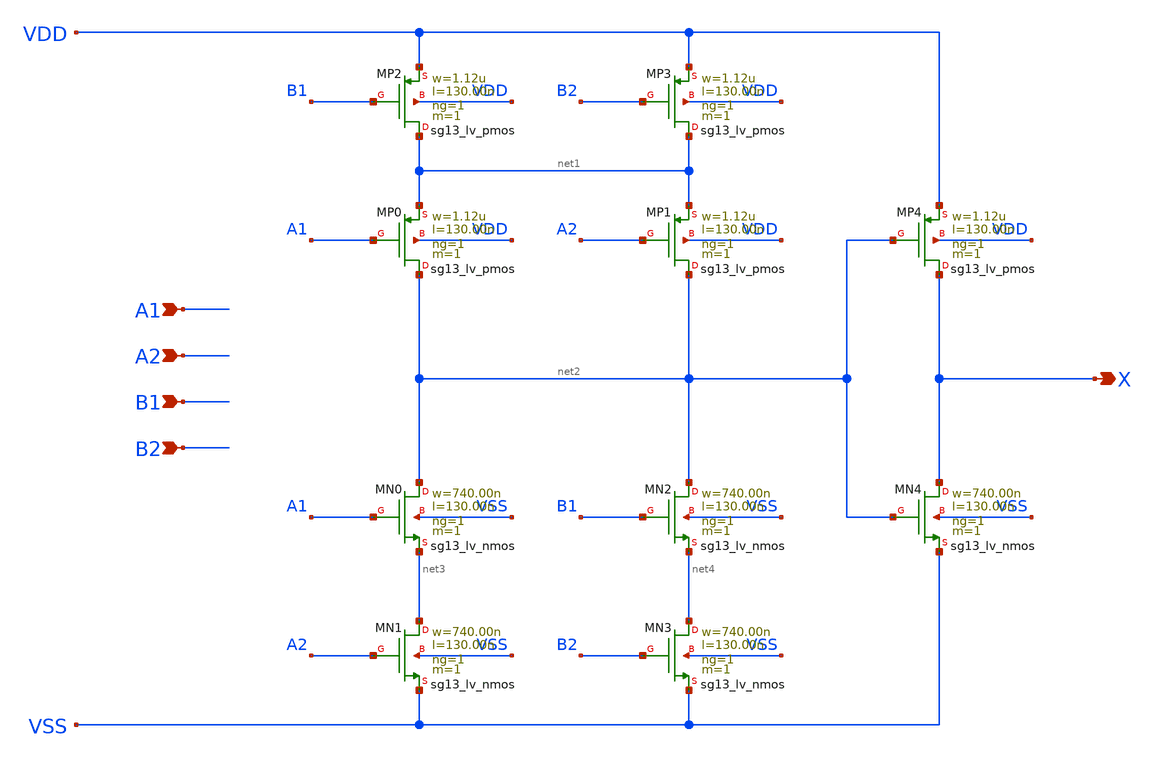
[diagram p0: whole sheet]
** sch_path: outputs/sg13g2_cells/cells/sg13g2_a22o_1/sg13g2_a22o_1.sch
**.subckt sg13g2_a22o_1 A1 A2 B1 B2 X
*.ipin A1
*.ipin A2
*.ipin B1
*.ipin B2
*.opin X
XMN0 net2 A1 net3 VSS sg13_lv_nmos w=740.00n l=130.00n ng=1 m=1 mm_ok=1
XMN1 net3 A2 VSS VSS sg13_lv_nmos w=740.00n l=130.00n ng=1 m=1 mm_ok=1
XMN2 net2 B1 net4 VSS sg13_lv_nmos w=740.00n l=130.00n ng=1 m=1 mm_ok=1
XMN3 net4 B2 VSS VSS sg13_lv_nmos w=740.00n l=130.00n ng=1 m=1 mm_ok=1
XMN4 X net2 VSS VSS sg13_lv_nmos w=740.00n l=130.00n ng=1 m=1 mm_ok=1
XMP0 net2 A1 net1 VDD sg13_lv_pmos w=1.12u l=130.00n ng=1 m=1 mm_ok=1
XMP1 net2 A2 net1 VDD sg13_lv_pmos w=1.12u l=130.00n ng=1 m=1 mm_ok=1
XMP2 net1 B1 VDD VDD sg13_lv_pmos w=1.12u l=130.00n ng=1 m=1 mm_ok=1
XMP3 net1 B2 VDD VDD sg13_lv_pmos w=1.12u l=130.00n ng=1 m=1 mm_ok=1
XMP4 X net2 VDD VDD sg13_lv_pmos w=1.12u l=130.00n ng=1 m=1 mm_ok=1
**.ends
.end
